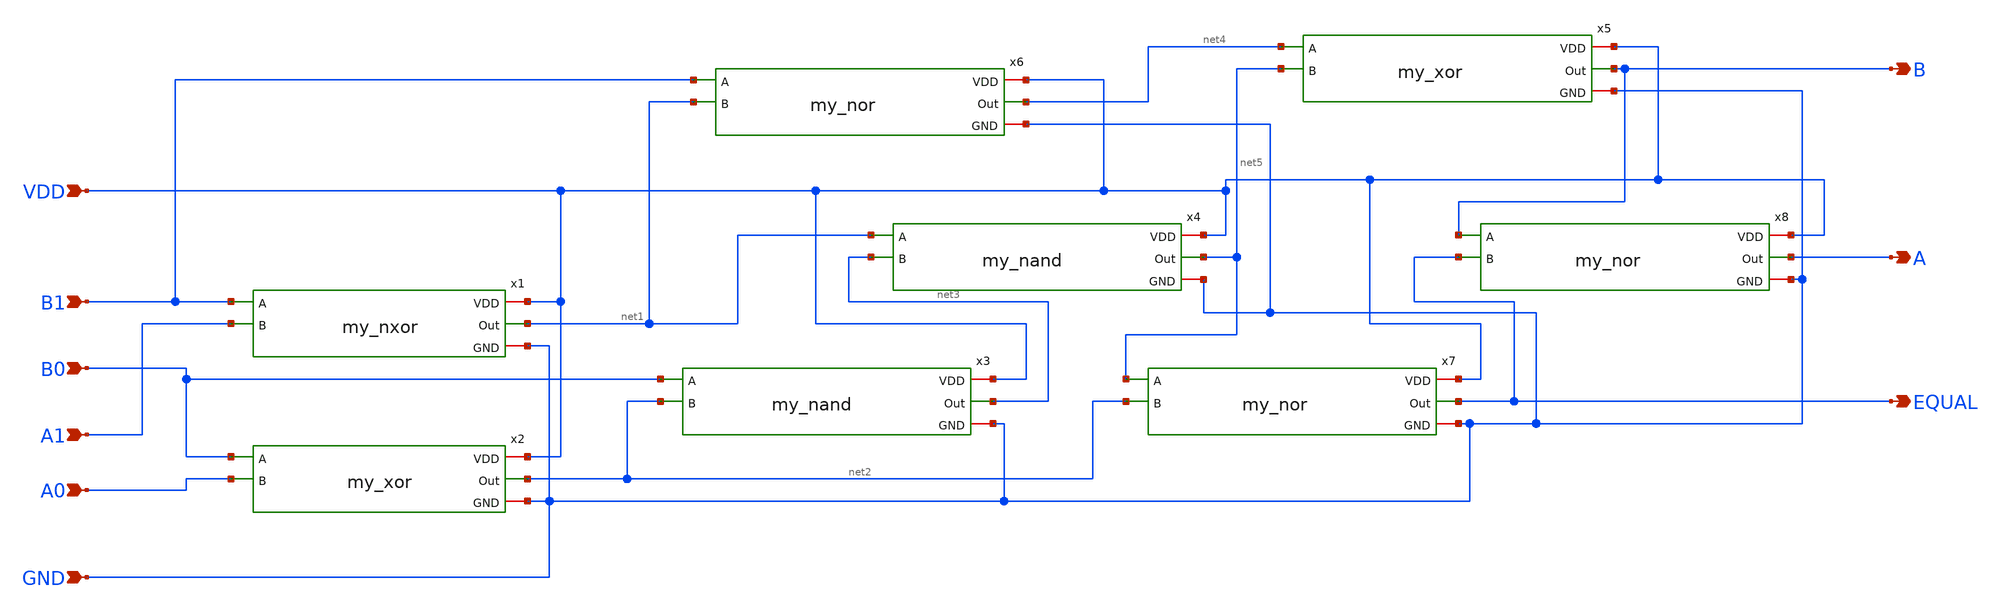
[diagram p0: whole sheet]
** sch_path: cells/comp4/2x_drive/2bit_comps_2x.sch
**.subckt 2bit_comps_2x VDD B1 B0 A1 GND A0 B A EQUAL
*.ipin VDD
*.ipin B1
*.ipin B0
*.ipin A1
*.ipin GND
*.ipin A0
*.opin B
*.opin A
*.opin EQUAL
x1 VDD B1 net1 A1 GND my_nxor
x2 VDD B0 net2 A0 GND my_xor
x3 VDD B0 net2 net3 GND my_nand
x4 VDD net1 net3 net5 GND my_nand
x5 VDD net4 B net5 GND my_xor
x6 VDD B1 net1 net4 GND my_nor
x7 VDD net5 net2 EQUAL GND my_nor
x8 VDD B EQUAL A GND my_nor
**.ends
.end
